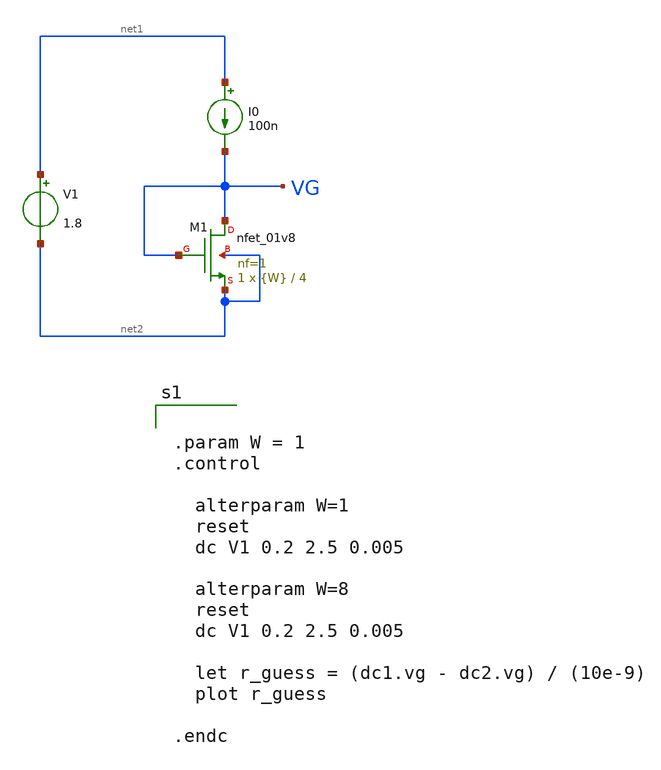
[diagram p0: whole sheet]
** sch_path: schem/bias/bias_bmr_r_guess.sch
**.subckt bias_bmr_r_guess
V1 net1 net2 1.8
I0 net1 VG 100n
XM1 VG VG net2 net2 sky130_fd_pr__nfet_01v8 L=4 W={W} nf=1 ad='int((1 + 1)/2) * {W} / 1 * 0.29' as='int((1 + 2)/2) * {W} / 1 * 0.29'
+ pd='2*int((1 + 1)/2) * ({W} / 1 + 0.29)' ps='2*int((1 + 2)/2) * ({W} / 1 + 0.29)' nrd='0.29 / {W} ' nrs='0.29 / {W} '
+ sa=0 sb=0 sd=0 mult=1 m=1
**** begin user architecture code

** opencircuitdesign pdks install
.lib $::SKYWATER_MODELS/sky130.lib.spice tt



.param W = 1
.control

  alterparam W=1
  reset
  dc V1 0.2 2.5 0.005

  alterparam W=8
  reset
  dc V1 0.2 2.5 0.005

  let r_guess = (dc1.vg - dc2.vg) / (10e-9)
  plot r_guess

.endc


**** end user architecture code
**.ends
.end
